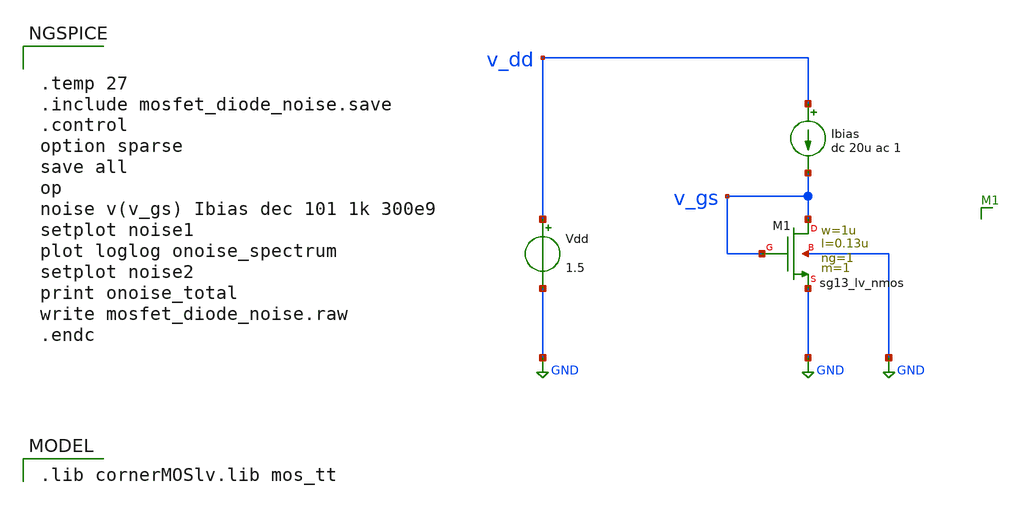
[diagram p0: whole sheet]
** sch_path: xschem/mosfet_diode_noise.sch
* (c) 2024-2025 Harald Pretl, Apache-2.0 license
**.subckt mosfet_diode_noise
Vdd v_dd GND 1.5
XM1 v_gs v_gs GND GND sg13_lv_nmos w=1u l=0.13u ng=1 m=1 mm_ok=1
Ibias v_dd v_gs dc 20u ac 1
**** begin user architecture code
 .lib cornerMOSlv.lib mos_tt



.temp 27
.include mosfet_diode_noise.save
.control
option sparse
save all
op
noise v(v_gs) Ibias dec 101 1k 300e9
setplot noise1
plot loglog onoise_spectrum
setplot noise2
print onoise_total
write mosfet_diode_noise.raw
.endc


**** end user architecture code
**.ends
.GLOBAL GND
.end
